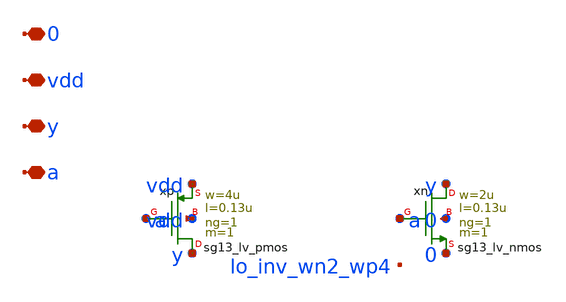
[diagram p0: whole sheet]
** sch_path: analog/lo/sch/lo_inv_2_4.sch
**.subckt lo_inv_2_4 a y vdd 0
*.iopin a
*.iopin y
*.iopin vdd
*.iopin 0
Xxp y a vdd vdd sg13_lv_pmos w=4u l=0.13u ng=1 m=1 mm_ok=1
Xxn y a 0 0 sg13_lv_nmos w=2u l=0.13u ng=1 m=1 mm_ok=1
**.ends
.end
